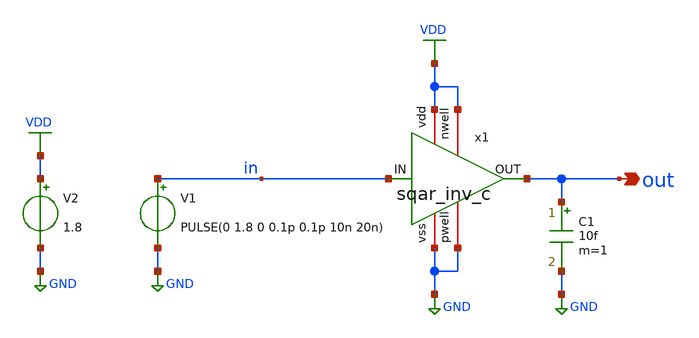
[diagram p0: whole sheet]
** sch_path: design/test/squ_inv_test.sch
**.subckt squ_inv_test out
*.opin out
V1 in GND PULSE(0 1.8 0 0.1p 0.1p 10n 20n)
V2 VDD GND 1.8
x1 VDD VDD out in GND GND sqar_inv_c
C1 out GND 10f m=1
**** begin user architecture code


.param temp=27



*.op
*.ac dec 10 1 10G
.tran 0.01n 50n


.save all




.options wnflag=1
.include $::SKYWATER_MODELS/cells/nfet_01v8/sky130_fd_pr__nfet_01v8__tt.corner.spice
.include $::SKYWATER_MODELS/cells/nfet_01v8_lvt/sky130_fd_pr__nfet_01v8_lvt__tt.corner.spice
.include $::SKYWATER_MODELS/cells/pfet_01v8/sky130_fd_pr__pfet_01v8__tt.corner.spice
*.include $::SKYWATER_MODELS/cells/nfet_03v3_nvt/sky130_fd_pr__nfet_03v3_nvt__tt.corner.spice
*.include $::SKYWATER_MODELS/cells/nfet_05v0_nvt/sky130_fd_pr__nfet_05v0_nvt__tt.corner.spice
.include $::SKYWATER_MODELS/cells/esd_nfet_01v8/sky130_fd_pr__esd_nfet_01v8__tt.corner.spice
.include $::SKYWATER_MODELS/cells/pfet_01v8_lvt/sky130_fd_pr__pfet_01v8_lvt__tt.corner.spice
*.include $::SKYWATER_MODELS/cells/pfet_01v8_hvt/sky130_fd_pr__pfet_01v8_hvt__tt.corner.spice
*.include $::SKYWATER_MODELS/cells/esd_pfet_g5v0d10v5/sky130_fd_pr__esd_pfet_g5v0d10v5__tt.corner.spice
*.include $::SKYWATER_MODELS/cells/pfet_g5v0d10v5/sky130_fd_pr__pfet_g5v0d10v5__tt.corner.spice
*.include $::SKYWATER_MODELS/cells/pfet_g5v0d16v0/sky130_fd_pr__pfet_g5v0d16v0__tt.corner.spice
*.include $::SKYWATER_MODELS/cells/nfet_g5v0d10v5/sky130_fd_pr__nfet_g5v0d10v5__tt.corner.spice
*.include $::SKYWATER_MODELS/cells/nfet_g5v0d16v0/sky130_fd_pr__nfet_g5v0d16v0__tt_discrete.corner.spice
*.include $::SKYWATER_MODELS/cells/esd_nfet_g5v0d10v5/sky130_fd_pr__esd_nfet_g5v0d10v5__tt.corner.spice
.include $::SKYWATER_MODELS/models/corners/tt/nonfet.spice
* Mismatch parameters
.include $::SKYWATER_MODELS/cells/nfet_01v8/sky130_fd_pr__nfet_01v8__mismatch.corner.spice
.include $::SKYWATER_MODELS/cells/pfet_01v8/sky130_fd_pr__pfet_01v8__mismatch.corner.spice
.include $::SKYWATER_MODELS/cells/nfet_01v8_lvt/sky130_fd_pr__nfet_01v8_lvt__mismatch.corner.spice
.include $::SKYWATER_MODELS/cells/pfet_01v8_lvt/sky130_fd_pr__pfet_01v8_lvt__mismatch.corner.spice
*.include $::SKYWATER_MODELS/cells/pfet_01v8_hvt/sky130_fd_pr__pfet_01v8_hvt__mismatch.corner.spice
*.include $::SKYWATER_MODELS/cells/nfet_g5v0d10v5/sky130_fd_pr__nfet_g5v0d10v5__mismatch.corner.spice
*.include $::SKYWATER_MODELS/cells/pfet_g5v0d10v5/sky130_fd_pr__pfet_g5v0d10v5__mismatch.corner.spice
*.include $::SKYWATER_MODELS/cells/nfet_05v0_nvt/sky130_fd_pr__nfet_05v0_nvt__mismatch.corner.spice
*.include $::SKYWATER_MODELS/cells/nfet_03v3_nvt/sky130_fd_pr__nfet_03v3_nvt__mismatch.corner.spice
* Resistor$::SKYWATER_MODELS/Capacitor
.include $::SKYWATER_MODELS/models/r+c/res_typical__cap_typical.spice
.include $::SKYWATER_MODELS/models/r+c/res_typical__cap_typical__lin.spice
* Special cells
*.include $::SKYWATER_MODELS/models/corners/tt/specialized_cells.spice
* All models
.include $::SKYWATER_MODELS/models/all.spice
* Corner
.include $::SKYWATER_MODELS/models/corners/tt/rf.spice

* Manually adding standard cell models
.include /pdk/open_pdks/install/share/pdk/sky130A/libs.ref/sky130_fd_sc_hs/spice/sky130_fd_sc_hs.spice

**** end user architecture code
**.ends
.GLOBAL GND
.GLOBAL VDD
.end
